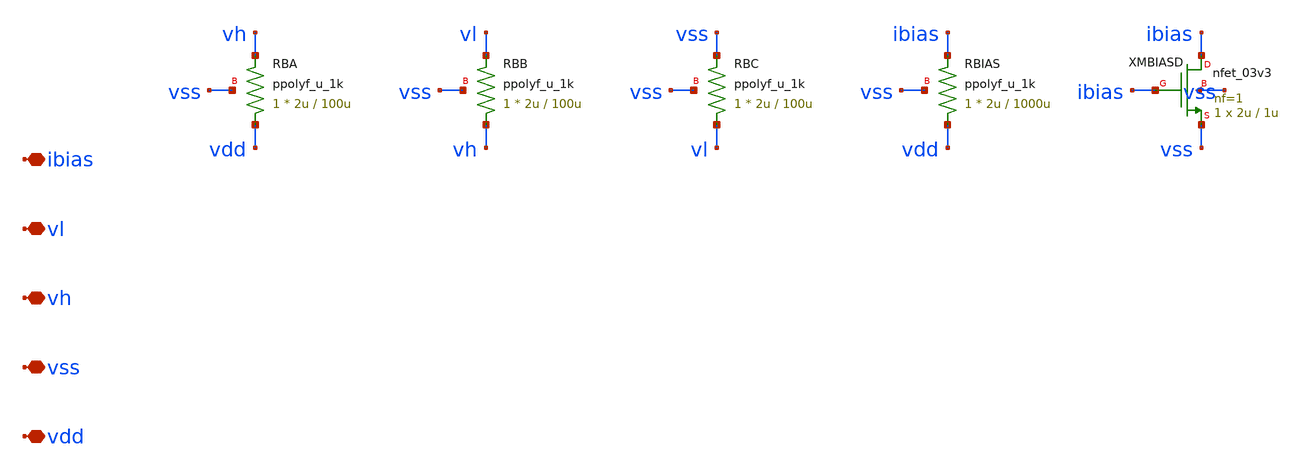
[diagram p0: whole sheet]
** sch_path: design/rcosc_bias.sch
**.subckt rcosc_bias vdd vss vh vl ibias
*.iopin vdd
*.iopin vss
*.iopin vh
*.iopin vl
*.iopin ibias
XRBA vdd vh vss ppolyf_u_1k r_width=2u r_length=100u m=1
XRBB vh vl vss ppolyf_u_1k r_width=2u r_length=100u m=1
XRBC vl vss vss ppolyf_u_1k r_width=2u r_length=100u m=1
XRBIAS vdd ibias vss ppolyf_u_1k r_width=2u r_length=1000u m=1
XMBIASD ibias ibias vss vss nfet_03v3 L=1u W=2u nf=1 ad='int((nf+1)/2) * W/nf * 0.18u' as='int((nf+2)/2) * W/nf * 0.18u'
+ pd='2*int((nf+1)/2) * (W/nf + 0.18u)' ps='2*int((nf+2)/2) * (W/nf + 0.18u)' nrd='0.18u / W' nrs='0.18u / W'
+ sa=0 sb=0 sd=0 m=1
**.ends
.end
